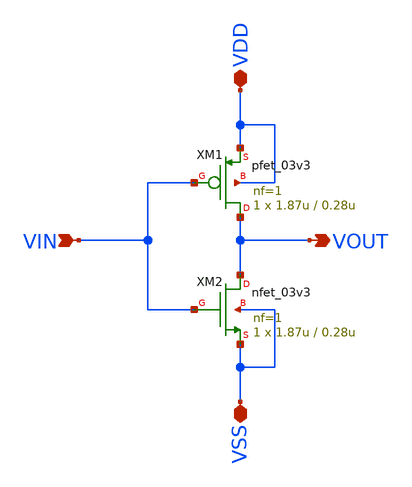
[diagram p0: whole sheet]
** sch_path: ABC123_SDC/design_data/xschem/INV/INV.sch
**.subckt INV VIN VDD VSS VOUT
*.ipin VIN
*.iopin VDD
*.iopin VSS
*.opin VOUT
XM1 VOUT VIN VDD VDD pfet_03v3 L=0.28u W=1.87u nf=1 ad='int((nf+1)/2) * W/nf * 0.18u' as='int((nf+2)/2) * W/nf * 0.18u'
+ pd='2*int((nf+1)/2) * (W/nf + 0.18u)' ps='2*int((nf+2)/2) * (W/nf + 0.18u)' nrd='0.18u / W' nrs='0.18u / W'
+ sa=0 sb=0 sd=0 m=1
XM2 VOUT VIN VSS VSS nfet_03v3 L=0.28u W=1.87u nf=1 ad='int((nf+1)/2) * W/nf * 0.18u' as='int((nf+2)/2) * W/nf * 0.18u'
+ pd='2*int((nf+1)/2) * (W/nf + 0.18u)' ps='2*int((nf+2)/2) * (W/nf + 0.18u)' nrd='0.18u / W' nrs='0.18u / W'
+ sa=0 sb=0 sd=0 m=1
**.ends
.end
